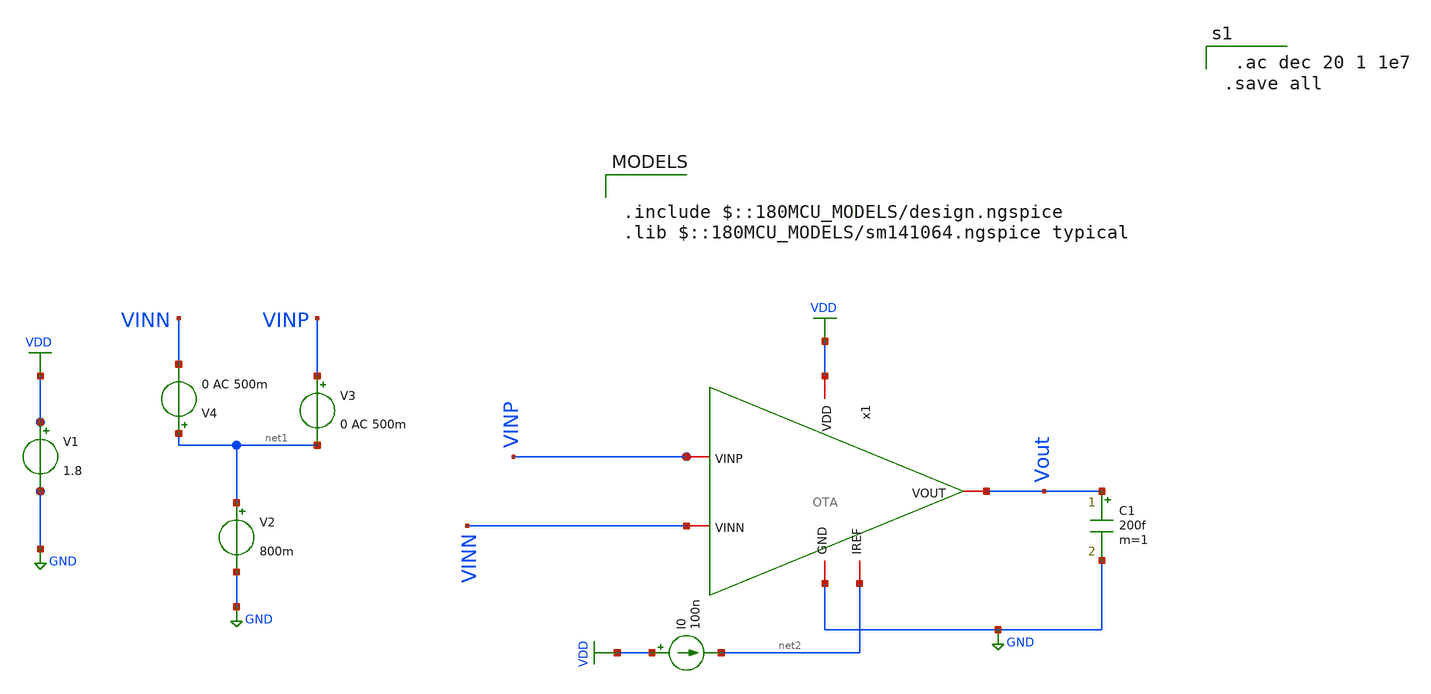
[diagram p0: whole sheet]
** sch_path: src/Pixel/OpAmpTb.sch
**.subckt OpAmpTb
C1 Vout GND 200f m=1
V1 VDD GND 1.8
V3 VINP net1 0 AC 500m
V4 net1 VINN 0 AC 500m
I0 VDD net2 100n
V2 net1 GND 800m
x1 VDD Vout VINP VINN net2 GND OTA
**** begin user architecture code

.include $::180MCU_MODELS/design.ngspice
.lib $::180MCU_MODELS/sm141064.ngspice typical


 .ac dec 20 1 1e7
.save all

**** end user architecture code
**.ends
.GLOBAL GND
.GLOBAL VDD
.end
